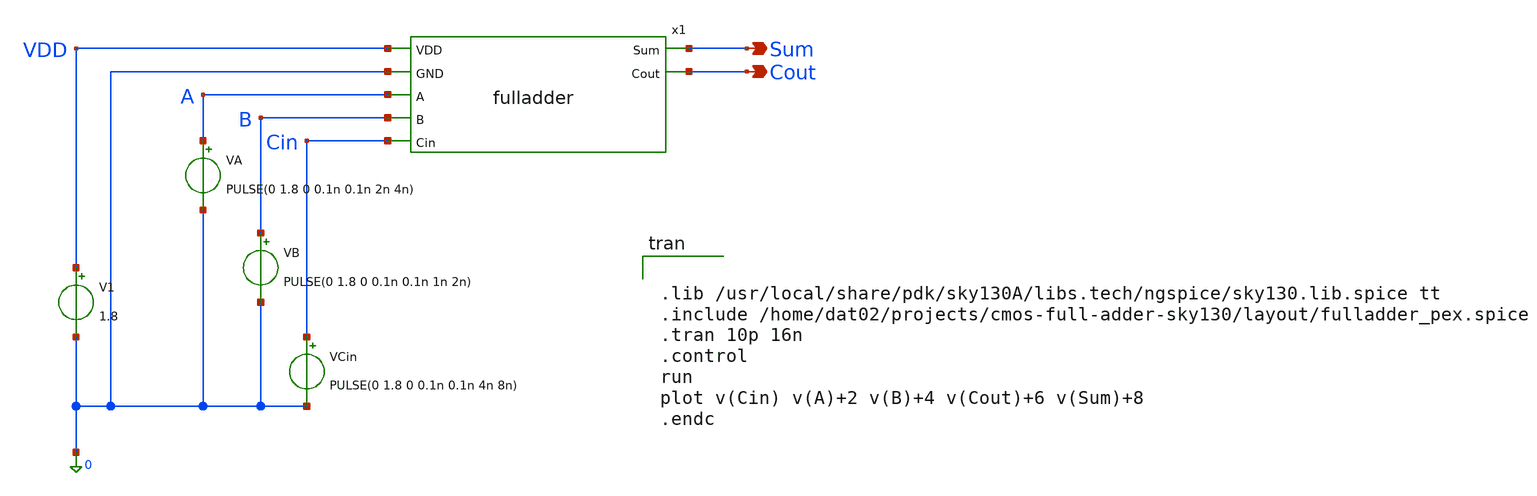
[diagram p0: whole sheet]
** sch_path: static_cmos/testbench/fa_tb_tran.sch
**.subckt fa_tb_tran Cout Sum
*.opin Cout
*.opin Sum
V1 VDD 0 1.8
VA A 0 PULSE(0 1.8 0 0.1n 0.1n 2n 4n)
VB B 0 PULSE(0 1.8 0 0.1n 0.1n 1n 2n)
VCin Cin 0 PULSE(0 1.8 0 0.1n 0.1n 4n 8n)
x1 VDD 0 Sum A B Cin Cout fulladder
**** begin user architecture code


.lib /usr/local/share/pdk/sky130A/libs.tech/ngspice/sky130.lib.spice tt
.include /home/dat02/projects/cmos-full-adder-sky130/layout/fulladder_pex.spice
.tran 10p 16n
.control
run
plot v(Cin) v(A)+2 v(B)+4 v(Cout)+6 v(Sum)+8
.endc


**** end user architecture code
**.ends
.end
